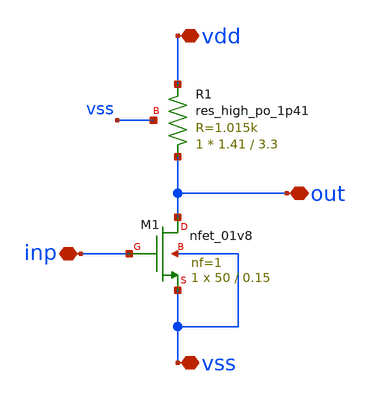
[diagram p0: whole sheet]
** sch_path: xschem/untitled-3.sch
**.subckt untitled-3 inp out vdd vss
*.iopin inp
*.iopin out
*.iopin vdd
*.iopin vss
XM1 out inp vss vss sky130_fd_pr__nfet_01v8 L=0.15 W=50 nf=1 ad='int((nf+1)/2) * W/nf * 0.29' as='int((nf+2)/2) * W/nf * 0.29'
+ pd='2*int((nf+1)/2) * (W/nf + 0.29)' ps='2*int((nf+2)/2) * (W/nf + 0.29)' nrd='0.29 / W' nrs='0.29 / W'
+ sa=0 sb=0 sd=0 mult=1 m=1
XR1 out vdd vss sky130_fd_pr__res_high_po_1p41 L=3.3 mult=1 m=1
**.ends
.end
